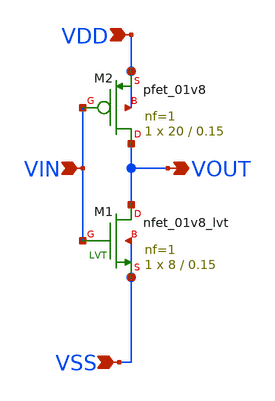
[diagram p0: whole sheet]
** sch_path: design/LELO_SVOD_SKY130A/LELO_INV_PVT2.sch
**.subckt LELO_INV_PVT2 VIN VDD VSS VOUT
*.ipin VIN
*.ipin VDD
*.ipin VSS
*.opin VOUT
XM1 VOUT VIN VSS VSS sky130_fd_pr__nfet_01v8_lvt L=0.15 W=8 nf=1 ad='int((1 + 1)/2) * 8 / 1 * 0.29' as='int((1 + 2)/2) * 8 / 1 * 0.29'
+ pd='2*int((1 + 1)/2) * (8 / 1 + 0.29)' ps='2*int((1 + 2)/2) * (8 / 1 + 0.29)' nrd='0.29 / 8 ' nrs='0.29 / 8 '
+ sa=0 sb=0 sd=0 mult=1 m=1
XM2 VOUT VIN VDD VDD sky130_fd_pr__pfet_01v8 L=0.15 W=20 nf=1 ad='int((1 + 1)/2) * 20 / 1 * 0.29' as='int((1 + 2)/2) * 20 / 1 * 0.29'
+ pd='2*int((1 + 1)/2) * (20 / 1 + 0.29)' ps='2*int((1 + 2)/2) * (20 / 1 + 0.29)' nrd='0.29 / 20 ' nrs='0.29 / 20 '
+ sa=0 sb=0 sd=0 mult=1 m=1
**.ends
.end
